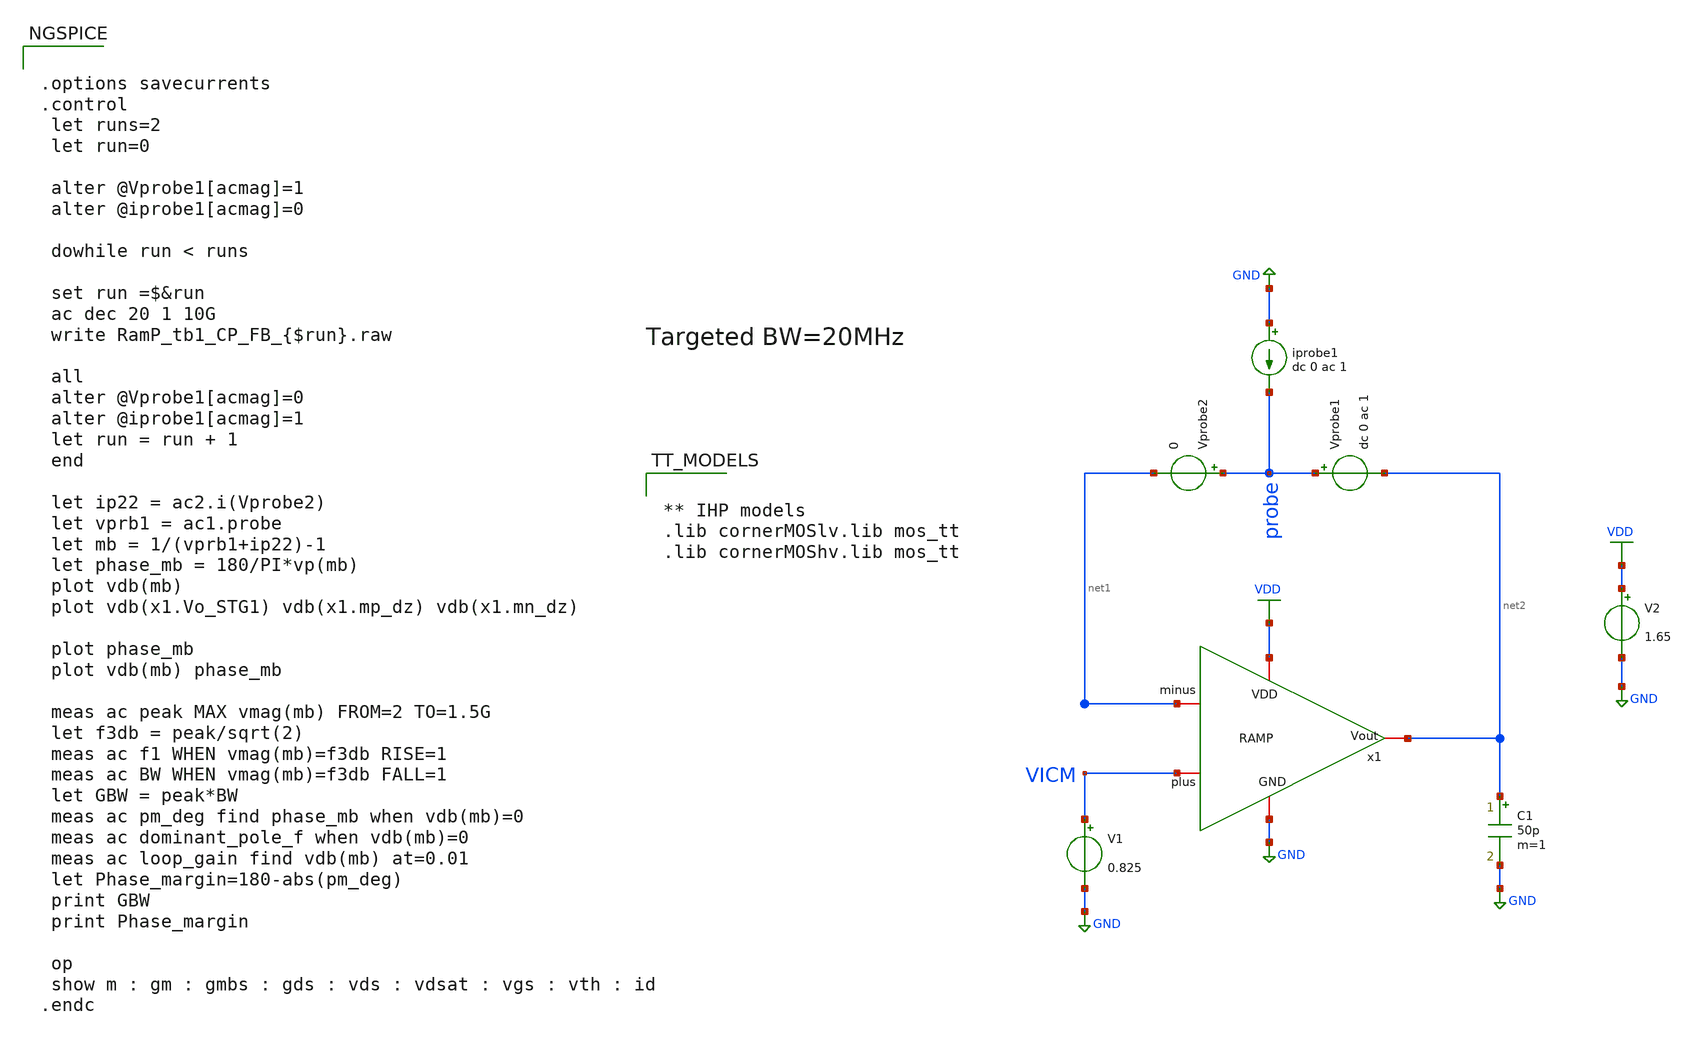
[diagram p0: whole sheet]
** sch_path: Design Files/RAMP/RAMP-Test/RamP_tb1_CP_FB.sch
**.subckt RamP_tb1_CP_FB
x1 VDD VICM net2 net1 GND RAMP
V1 VICM GND 0.825
V2 VDD GND 1.65
C1 net2 GND 50p m=1
Vprobe2 probe net1 0
Vprobe1 probe net2 dc 0 ac 1
iprobe1 GND probe dc 0 ac 1
**** begin user architecture code


.options savecurrents
.control
 let runs=2
 let run=0

 alter @Vprobe1[acmag]=1
 alter @iprobe1[acmag]=0

 dowhile run < runs

 set run =$&run
 ac dec 20 1 10G
 write RamP_tb1_CP_FB_{$run}.raw

 all
 alter @Vprobe1[acmag]=0
 alter @iprobe1[acmag]=1
 let run = run + 1
 end

 let ip22 = ac2.i(Vprobe2)
 let vprb1 = ac1.probe
 let mb = 1/(vprb1+ip22)-1
 let phase_mb = 180/PI*vp(mb)
 plot vdb(mb)
 plot vdb(x1.Vo_STG1) vdb(x1.mp_dz) vdb(x1.mn_dz)

 plot phase_mb
 plot vdb(mb) phase_mb

 meas ac peak MAX vmag(mb) FROM=2 TO=1.5G
 let f3db = peak/sqrt(2)
 meas ac f1 WHEN vmag(mb)=f3db RISE=1
 meas ac BW WHEN vmag(mb)=f3db FALL=1
 let GBW = peak*BW
 meas ac pm_deg find phase_mb when vdb(mb)=0
 meas ac dominant_pole_f when vdb(mb)=0
 meas ac loop_gain find vdb(mb) at=0.01
 let Phase_margin=180-abs(pm_deg)
 print GBW
 print Phase_margin

 op
 show m : gm : gmbs : gds : vds : vdsat : vgs : vth : id
.endc




** IHP models
.lib cornerMOSlv.lib mos_tt
.lib cornerMOShv.lib mos_tt


**** end user architecture code
**.ends

* expanding   symbol:  /foss/designs/RAMP/Fully-Diff-RAMP/RAMP.sym # of pins=5
** sym_path: Design Files/RAMP/Fully-Diff-RAMP/RAMP.sym
** sch_path: Design Files/RAMP/Fully-Diff-RAMP/RAMP.sch
.subckt RAMP VDD minus Vout plus GND
*.iopin GND
*.iopin plus
*.iopin minus
*.iopin Vout
*.iopin VDD
x1 VDD Vo_STG1 V1_CM plus minus GND STG1
x2 VDD net2 mp_dz Vo_STG1 mn_dz net1 GND STG2
XM1 Vout mn_dz GND GND sg13_hv_nmos w=2.3u l=1u ng=1 m=4 mm_ok=1
XM2 Vout mp_dz VDD VDD sg13_hv_pmos w=4.5u l=0.5u ng=1 m=4 mm_ok=1
x3 VDD net2 V1_CM net1 GND STG2_Replica
x4 VDD V1_CM GND STG1-CM
.ends


* expanding   symbol:  /foss/designs/RAMP/Fully-Diff-RAMP/STG1.sym # of pins=6
** sym_path: Design Files/RAMP/Fully-Diff-RAMP/STG1.sym
** sch_path: Design Files/RAMP/Fully-Diff-RAMP/STG1.sch
.subckt STG1 VDD Vo1 V1_CM Vin Vip GND
*.iopin VDD
*.iopin GND
*.opin Vo1
*.ipin Vip
*.ipin Vin
*.ipin V1_CM
R1 net3 net2 100k m=1
R3 net3 Vo1 100k m=1
XMN_STG1_IP_N1 net2 Vip net4 GND sg13_lv_nmos w=1.563u l=0.5u ng=1 m=2 mm_ok=1
XMN_STG1_IP_N2 Vo1 Vin net4 GND sg13_lv_nmos w=1.563u l=0.5u ng=1 m=2 mm_ok=1
I0 net4 GND 10u
XMP_STG1_CL_P1 net2 net1 VDD VDD sg13_hv_pmos w=0.5u l=1u ng=1 m=1 mm_ok=1
XMP_STG1_CL_P2 Vo1 net1 VDD VDD sg13_hv_pmos w=0.5u l=1u ng=1 m=1 mm_ok=1
E1 net1 GND net3 V1_CM 10k
.ends


* expanding   symbol:  /foss/designs/RAMP/Fully-Diff-RAMP/STG2.sym # of pins=7
** sym_path: Design Files/RAMP/Fully-Diff-RAMP/STG2.sym
** sch_path: Design Files/RAMP/Fully-Diff-RAMP/STG2.sch
.subckt STG2 VDD VCTRL_P VDZP Vin_2 VDZN VCTRL_N GND
*.ipin Vin_2
*.ipin VDD
*.ipin GND
*.ipin VCTRL_P
*.ipin VCTRL_N
*.opin VDZN
*.opin VDZP
XMN_STG2_3N1 VDZN Vin_2 GND GND sg13_lv_nmos w=0.15u l=0.13u ng=1 m=1 mm_ok=1
XMN_STG2_3P1 VDZN Vin_2 net1 VDD sg13_lv_pmos w=0.15u l=0.13u ng=1 m=3 mm_ok=1
XMP_DZ_STG2_3N net1 VCTRL_P VDD VDD sg13_lv_pmos w=0.15u l=0.13u ng=1 m=5 mm_ok=1
XMP_STG2_3P2 VDZP Vin_2 net2 net2 sg13_lv_nmos w=0.15u l=0.13u ng=1 m=1 mm_ok=1
XMP_STG2_3P1 VDZP Vin_2 VDD VDD sg13_lv_pmos w=0.15u l=0.13u ng=1 m=1 mm_ok=1
XMN_DZ_STG2_3P net2 VCTRL_N GND GND sg13_lv_nmos w=0.15u l=0.13u ng=1 m=1 mm_ok=1
.ends


* expanding   symbol:  /foss/designs/RAMP/Fully-Diff-RAMP/STG2_Replica.sym # of pins=5
** sym_path: Design Files/RAMP/Fully-Diff-RAMP/STG2_Replica.sym
** sch_path: Design Files/RAMP/Fully-Diff-RAMP/STG2_Replica.sch
.subckt STG2_Replica VDD VCTRLP Vin_STG2 VCTRLN GND
*.ipin Vin_STG2
*.iopin VDD
*.iopin GND
*.opin VCTRLP
*.opin VCTRLN
XMN_STG2_3N1 net1 Vin_STG2 GND GND sg13_lv_nmos w=0.15u l=0.13u ng=1 m=1 mm_ok=1
XMN_STG2_3P1 net1 Vin_STG2 net2 VDD sg13_lv_pmos w=0.15u l=0.13u ng=1 m=3 mm_ok=1
XMP_DZ_STG2_3N net2 VCTRLP VDD VDD sg13_lv_pmos w=0.15u l=0.13u ng=1 m=5 mm_ok=1
XMP_STG2_3P2 net4 Vin_STG2 net3 net3 sg13_lv_nmos w=0.15u l=0.13u ng=1 m=1 mm_ok=1
XMP_STG2_3P1 net4 Vin_STG2 VDD VDD sg13_lv_pmos w=0.15u l=0.13u ng=1 m=1 mm_ok=1
XMN_DZ_STG2_3P net3 VCTRLN GND GND sg13_lv_nmos w=0.15u l=0.13u ng=1 m=1 mm_ok=1
XMN_STG2_3N_R net5 net5 GND GND sg13_hv_nmos w=2.3u l=1u ng=1 m=1 mm_ok=1
I0 VDD net5 1u
x1 VDD net1 net5 VCTRLP GND POTA
XMP_STG2_3P_R net6 net6 VDD VDD sg13_hv_pmos w=4.5u l=0.5u ng=1 m=1 mm_ok=1
I1 net6 GND 1u
x2 VDD VCTRLN net4 net6 GND NOTA
.ends


* expanding   symbol:  /foss/designs/RAMP/Fully-Diff-RAMP/STG1-CM.sym # of pins=3
** sym_path: Design Files/RAMP/Fully-Diff-RAMP/STG1-CM.sym
** sch_path: Design Files/RAMP/Fully-Diff-RAMP/STG1-CM.sch
.subckt STG1-CM VDD V_CM1 GND
*.ipin VDD
*.ipin GND
*.opin V_CM1
XM9 V_CM1 V_CM1 GND GND sg13_lv_nmos w=0.15u l=0.13u ng=1 m=1 mm_ok=1
XM10 V_CM1 V_CM1 net1 VDD sg13_lv_pmos w=0.15u l=0.13u ng=1 m=3 mm_ok=1
XM11 net1 GND VDD VDD sg13_lv_pmos w=0.15u l=0.13u ng=1 m=5 mm_ok=1
XM12 V_CM1 V_CM1 net2 net2 sg13_lv_nmos w=0.15u l=0.13u ng=1 m=1 mm_ok=1
XM13 V_CM1 V_CM1 VDD VDD sg13_lv_pmos w=0.15u l=0.13u ng=1 m=1 mm_ok=1
XM14 net2 VDD GND GND sg13_lv_nmos w=0.15u l=0.13u ng=1 m=1 mm_ok=1
.ends


* expanding   symbol:  /foss/designs/RAMP/OTA/POTA.sym # of pins=5
** sym_path: Design Files/RAMP/OTA/POTA.sym
** sch_path: Design Files/RAMP/OTA/POTA.sch
.subckt POTA VDD PLUS MINUS Vout GND
*.ipin VDD
*.ipin GND
*.ipin PLUS
*.ipin MINUS
*.opin Vout
XM2 net2 PLUS net1 VDD sg13_lv_pmos w=1.2u l=0.5u ng=1 m=2 mm_ok=1
XM3 Vout MINUS net1 VDD sg13_lv_pmos w=1.2u l=0.5u ng=1 m=2 mm_ok=1
XM4 Vout net2 GND GND sg13_hv_nmos w=0.5u l=2u ng=1 m=1 mm_ok=1
XM5 net2 net2 GND GND sg13_hv_nmos w=0.5u l=2u ng=1 m=1 mm_ok=1
I1 VDD net1 2u
.ends


* expanding   symbol:  /foss/designs/RAMP/OTA/NOTA.sym # of pins=5
** sym_path: Design Files/RAMP/OTA/NOTA.sym
** sch_path: Design Files/RAMP/OTA/NOTA.sch
.subckt NOTA VDD Vout PLUS MINUS GND
*.ipin VDD
*.ipin GND
*.ipin PLUS
*.ipin MINUS
*.opin Vout
XM1 net2 PLUS net1 GND sg13_hv_nmos w=1.75u l=1u ng=1 m=2 mm_ok=1
XM2 Vout MINUS net1 GND sg13_hv_nmos w=1.75u l=1u ng=1 m=2 mm_ok=1
I0 net1 GND 2u
XM3 Vout net2 VDD VDD sg13_hv_pmos w=0.5u l=0.75u ng=1 m=1 mm_ok=1
XM4 net2 net2 VDD VDD sg13_hv_pmos w=0.5u l=0.75u ng=1 m=1 mm_ok=1
.ends

.GLOBAL VDD
.GLOBAL GND
.end
